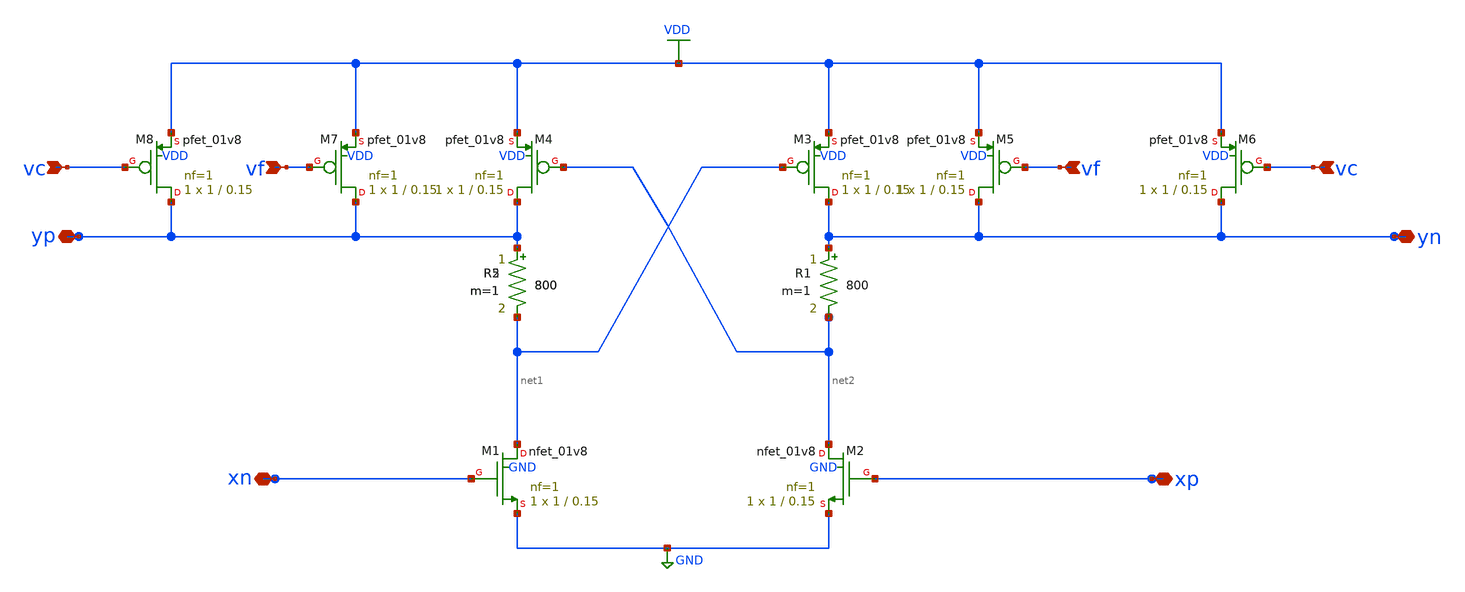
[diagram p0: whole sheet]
** sch_path: delay_cell/delay_cell_m.sch
**.subckt delay_cell_m yp xn xp yn vc vf vf vc
*.iopin yp
*.iopin xn
*.iopin xp
*.iopin yn
*.ipin vc
*.ipin vf
*.ipin vf
*.ipin vc
R2 yp net1 800 m=1
R1 yn net2 800 m=1
R5 yp net1 800 m=1
XM1 net1 xn GND GND sky130_fd_pr__nfet_01v8 L=0.15 W=1 nf=1 ad='int((nf+1)/2) * W/nf * 0.29' as='int((nf+2)/2) * W/nf * 0.29'
+ pd='2*int((nf+1)/2) * (W/nf + 0.29)' ps='2*int((nf+2)/2) * (W/nf + 0.29)' nrd='0.29 / W' nrs='0.29 / W'
+ sa=0 sb=0 sd=0 mult=1 m=1
XM2 net2 xp GND GND sky130_fd_pr__nfet_01v8 L=0.15 W=1 nf=1 ad='int((nf+1)/2) * W/nf * 0.29' as='int((nf+2)/2) * W/nf * 0.29'
+ pd='2*int((nf+1)/2) * (W/nf + 0.29)' ps='2*int((nf+2)/2) * (W/nf + 0.29)' nrd='0.29 / W' nrs='0.29 / W'
+ sa=0 sb=0 sd=0 mult=1 m=1
XM3 yn net1 VDD VDD sky130_fd_pr__pfet_01v8 L=0.15 W=1 nf=1 ad='int((nf+1)/2) * W/nf * 0.29' as='int((nf+2)/2) * W/nf * 0.29'
+ pd='2*int((nf+1)/2) * (W/nf + 0.29)' ps='2*int((nf+2)/2) * (W/nf + 0.29)' nrd='0.29 / W' nrs='0.29 / W'
+ sa=0 sb=0 sd=0 mult=1 m=1
XM4 yp net2 VDD VDD sky130_fd_pr__pfet_01v8 L=0.15 W=1 nf=1 ad='int((nf+1)/2) * W/nf * 0.29' as='int((nf+2)/2) * W/nf * 0.29'
+ pd='2*int((nf+1)/2) * (W/nf + 0.29)' ps='2*int((nf+2)/2) * (W/nf + 0.29)' nrd='0.29 / W' nrs='0.29 / W'
+ sa=0 sb=0 sd=0 mult=1 m=1
XM5 yn vf VDD VDD sky130_fd_pr__pfet_01v8 L=0.15 W=1 nf=1 ad='int((nf+1)/2) * W/nf * 0.29' as='int((nf+2)/2) * W/nf * 0.29'
+ pd='2*int((nf+1)/2) * (W/nf + 0.29)' ps='2*int((nf+2)/2) * (W/nf + 0.29)' nrd='0.29 / W' nrs='0.29 / W'
+ sa=0 sb=0 sd=0 mult=1 m=1
XM6 yn vc VDD VDD sky130_fd_pr__pfet_01v8 L=0.15 W=1 nf=1 ad='int((nf+1)/2) * W/nf * 0.29' as='int((nf+2)/2) * W/nf * 0.29'
+ pd='2*int((nf+1)/2) * (W/nf + 0.29)' ps='2*int((nf+2)/2) * (W/nf + 0.29)' nrd='0.29 / W' nrs='0.29 / W'
+ sa=0 sb=0 sd=0 mult=1 m=1
XM7 yp vf VDD VDD sky130_fd_pr__pfet_01v8 L=0.15 W=1 nf=1 ad='int((nf+1)/2) * W/nf * 0.29' as='int((nf+2)/2) * W/nf * 0.29'
+ pd='2*int((nf+1)/2) * (W/nf + 0.29)' ps='2*int((nf+2)/2) * (W/nf + 0.29)' nrd='0.29 / W' nrs='0.29 / W'
+ sa=0 sb=0 sd=0 mult=1 m=1
XM8 yp vc VDD VDD sky130_fd_pr__pfet_01v8 L=0.15 W=1 nf=1 ad='int((nf+1)/2) * W/nf * 0.29' as='int((nf+2)/2) * W/nf * 0.29'
+ pd='2*int((nf+1)/2) * (W/nf + 0.29)' ps='2*int((nf+2)/2) * (W/nf + 0.29)' nrd='0.29 / W' nrs='0.29 / W'
+ sa=0 sb=0 sd=0 mult=1 m=1
**.ends
.GLOBAL GND
.GLOBAL VDD
.end
